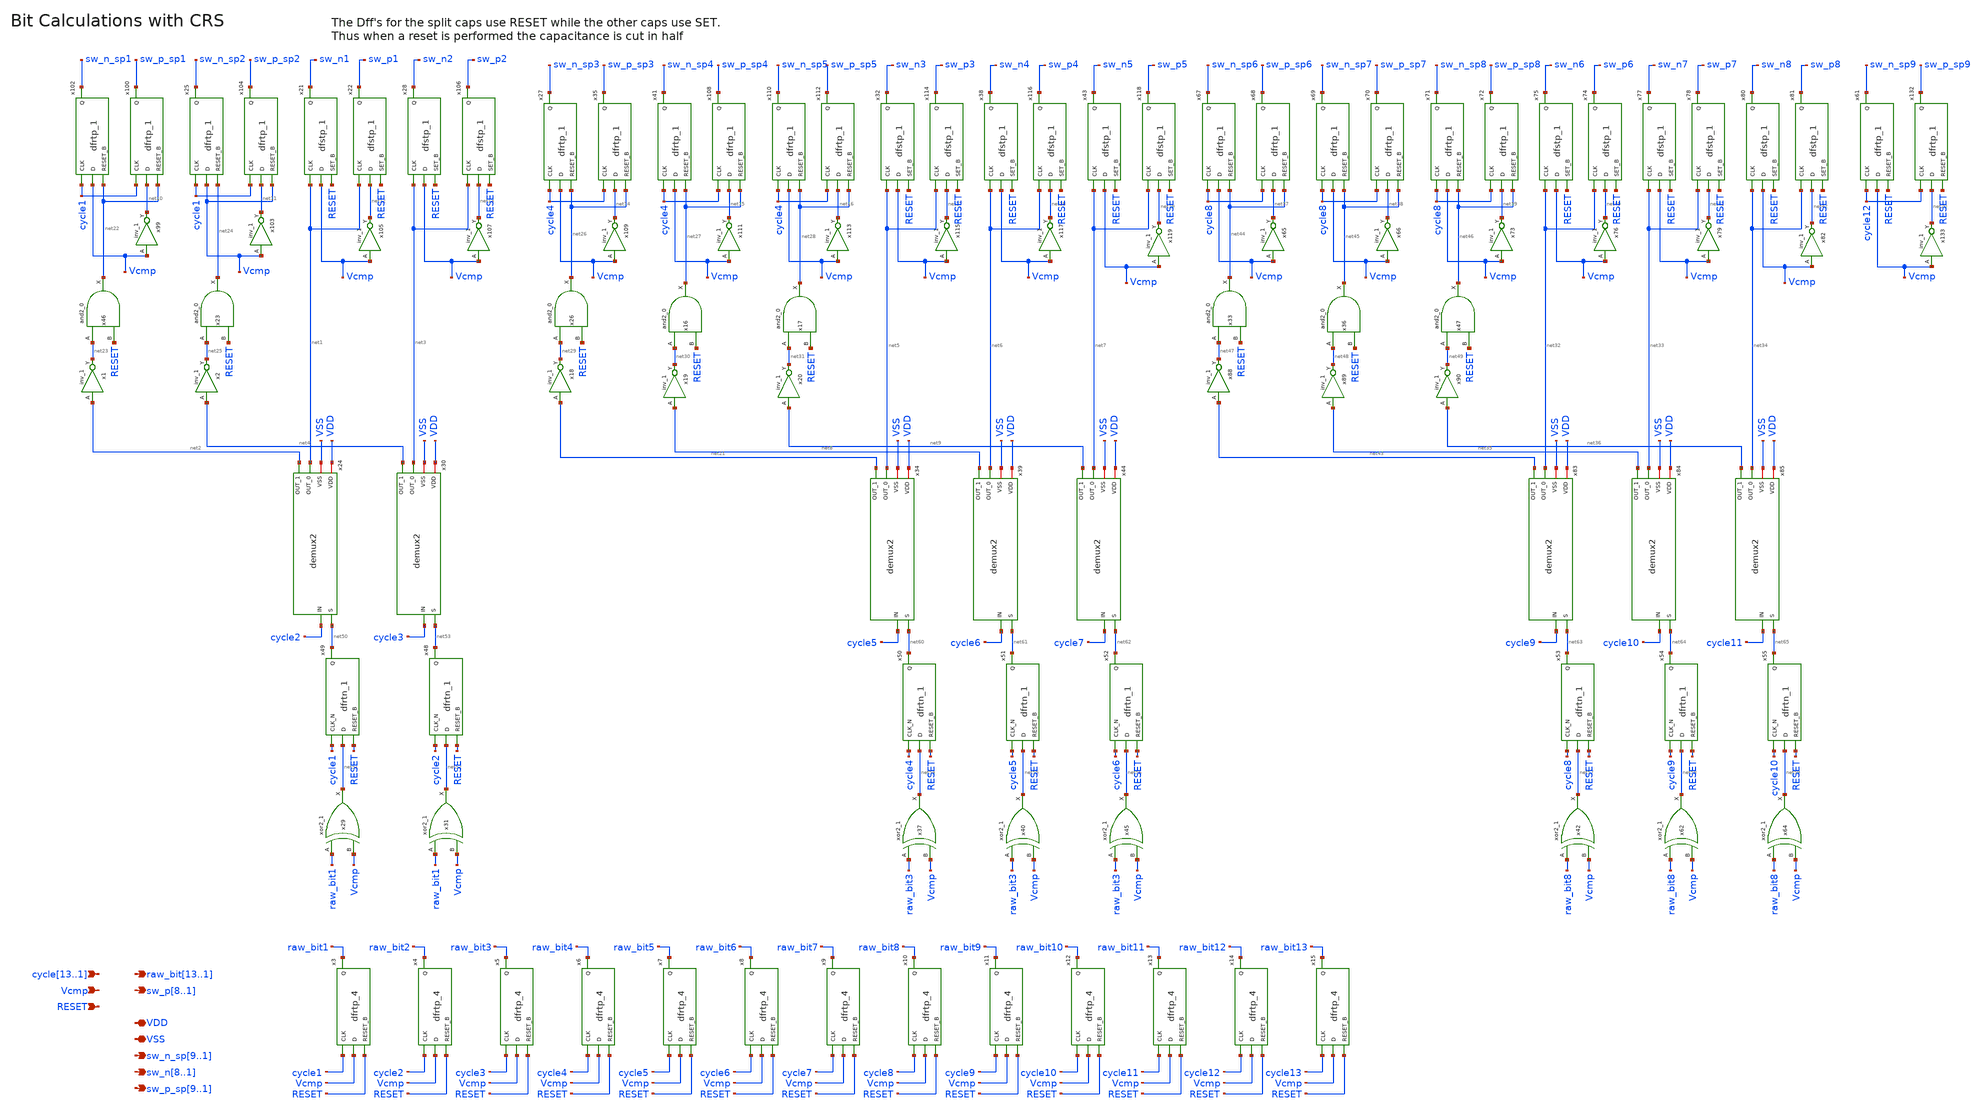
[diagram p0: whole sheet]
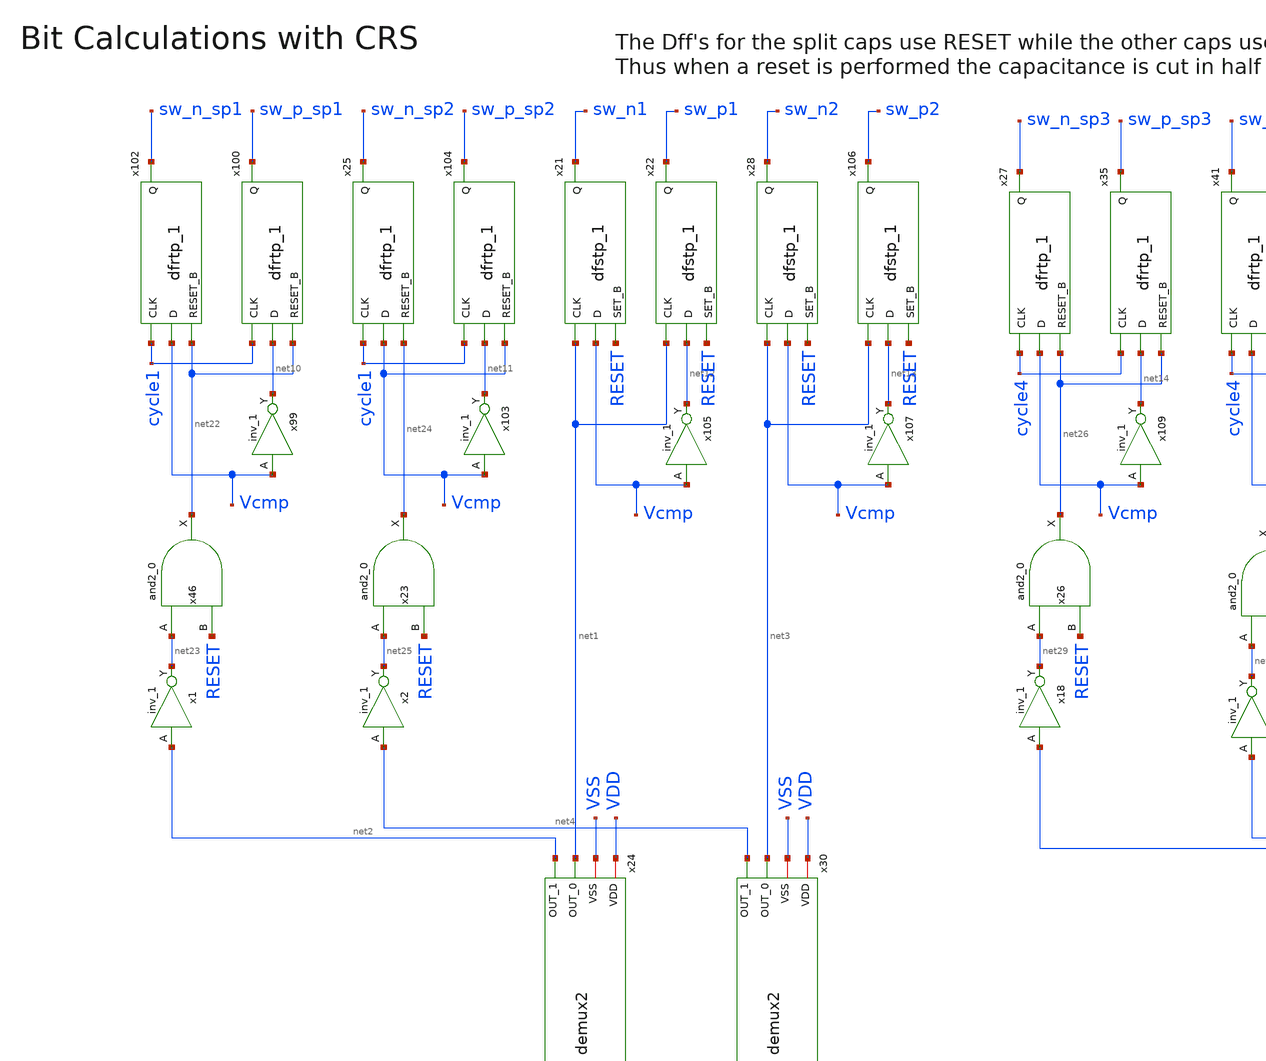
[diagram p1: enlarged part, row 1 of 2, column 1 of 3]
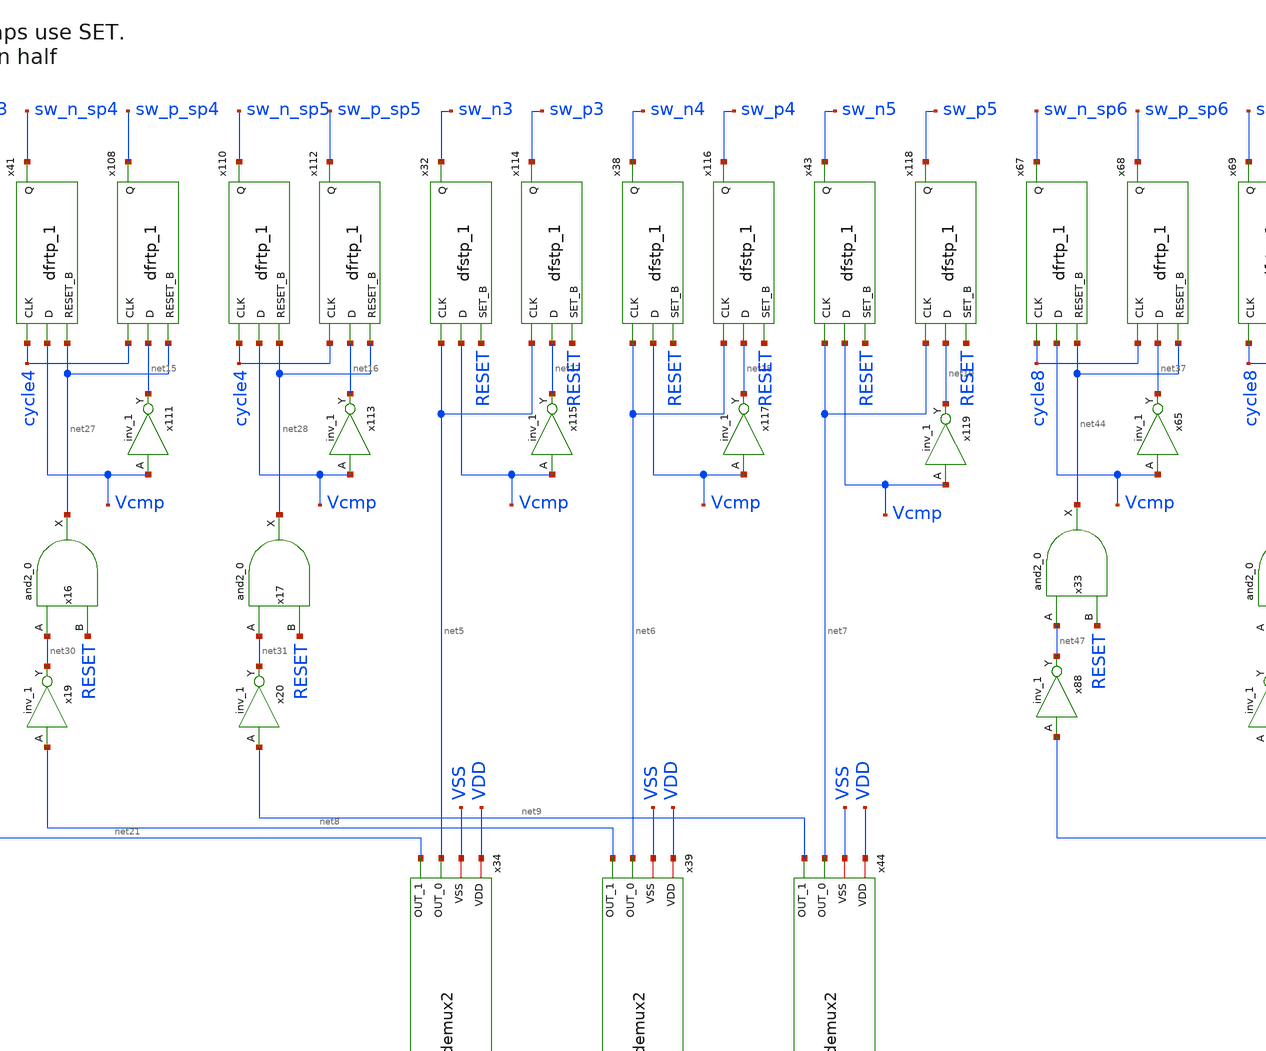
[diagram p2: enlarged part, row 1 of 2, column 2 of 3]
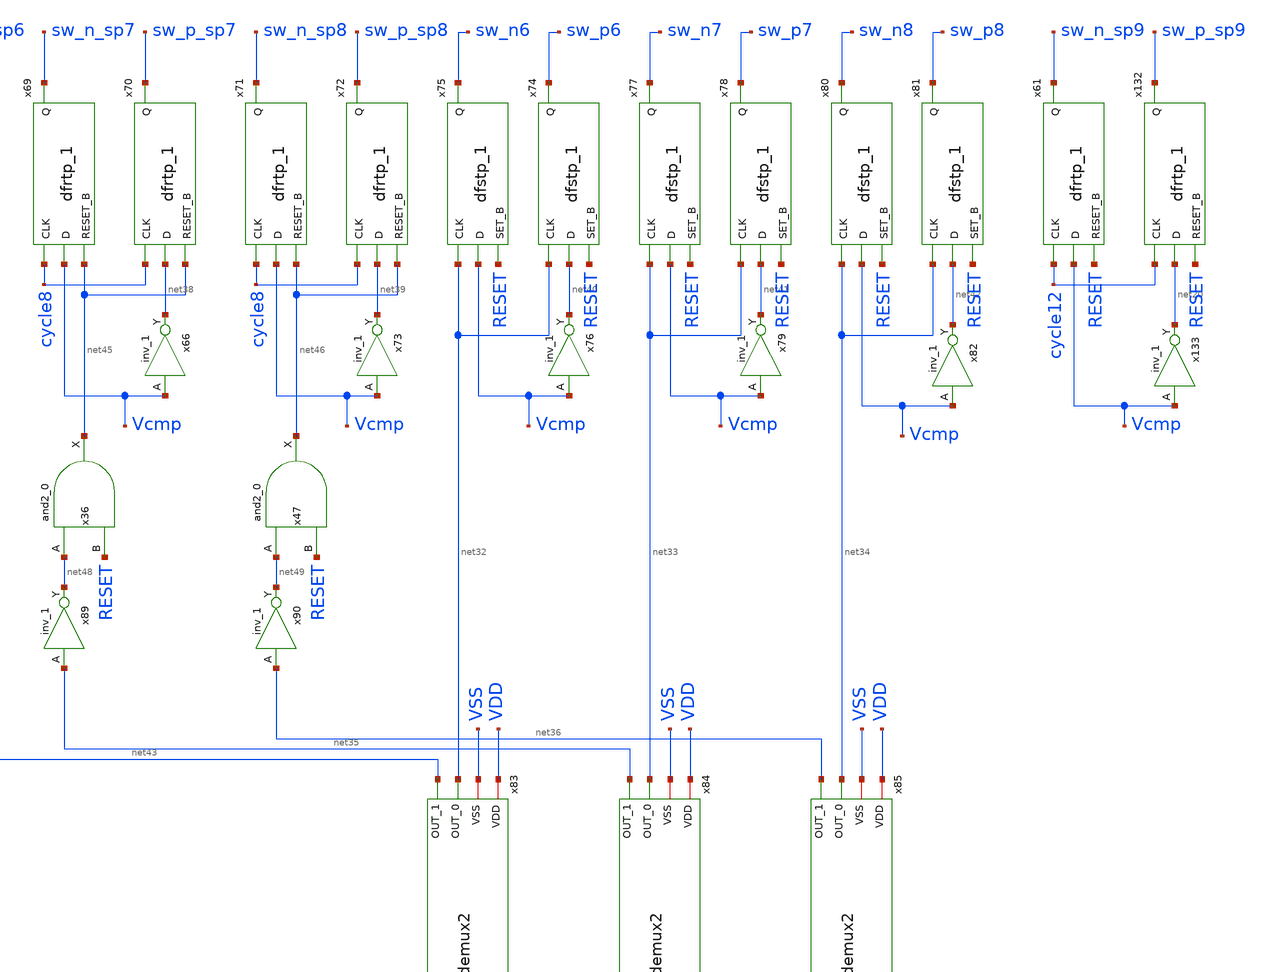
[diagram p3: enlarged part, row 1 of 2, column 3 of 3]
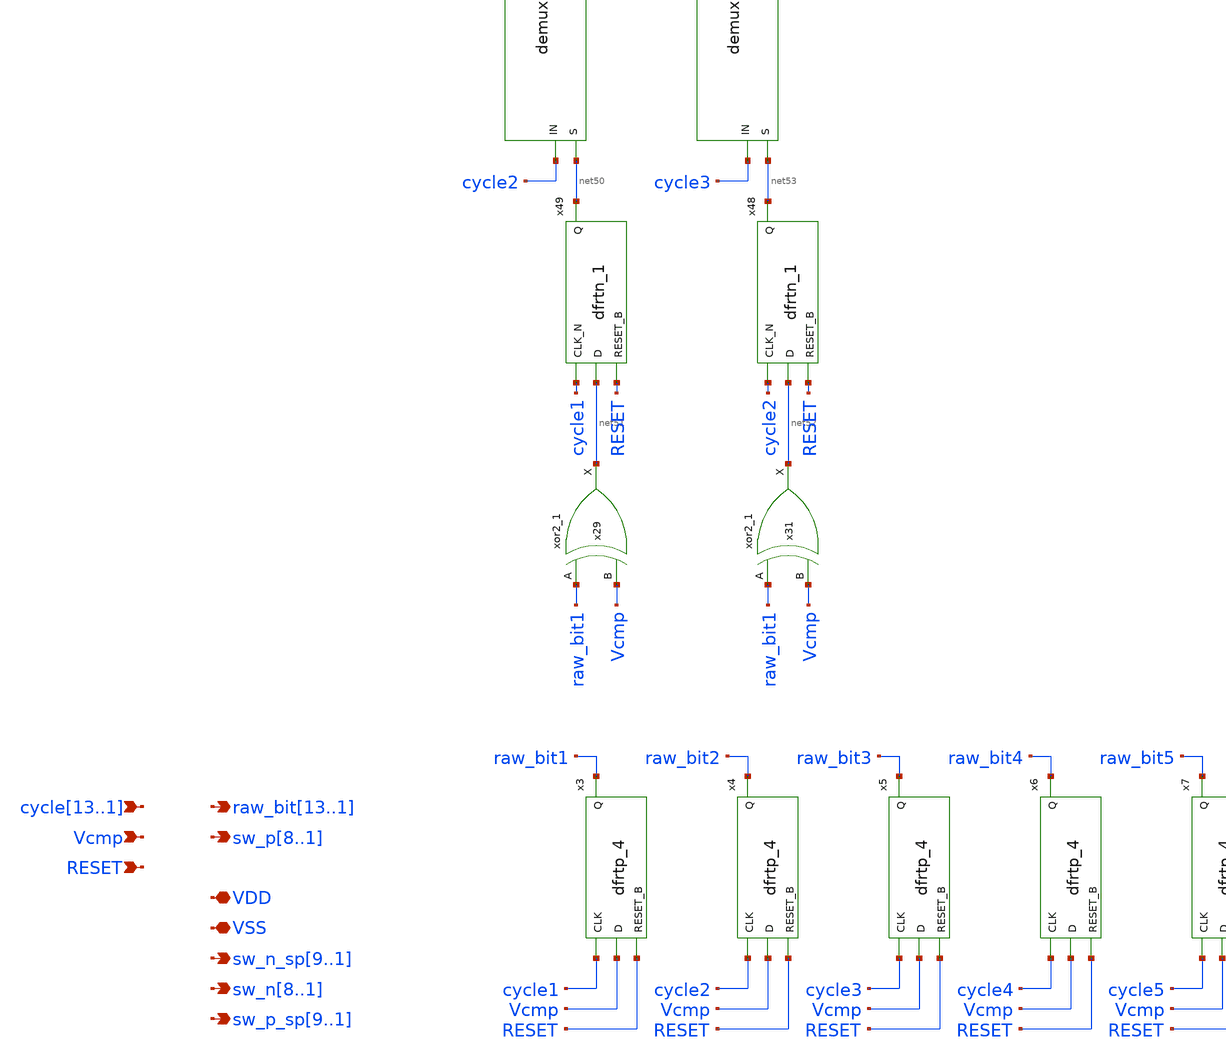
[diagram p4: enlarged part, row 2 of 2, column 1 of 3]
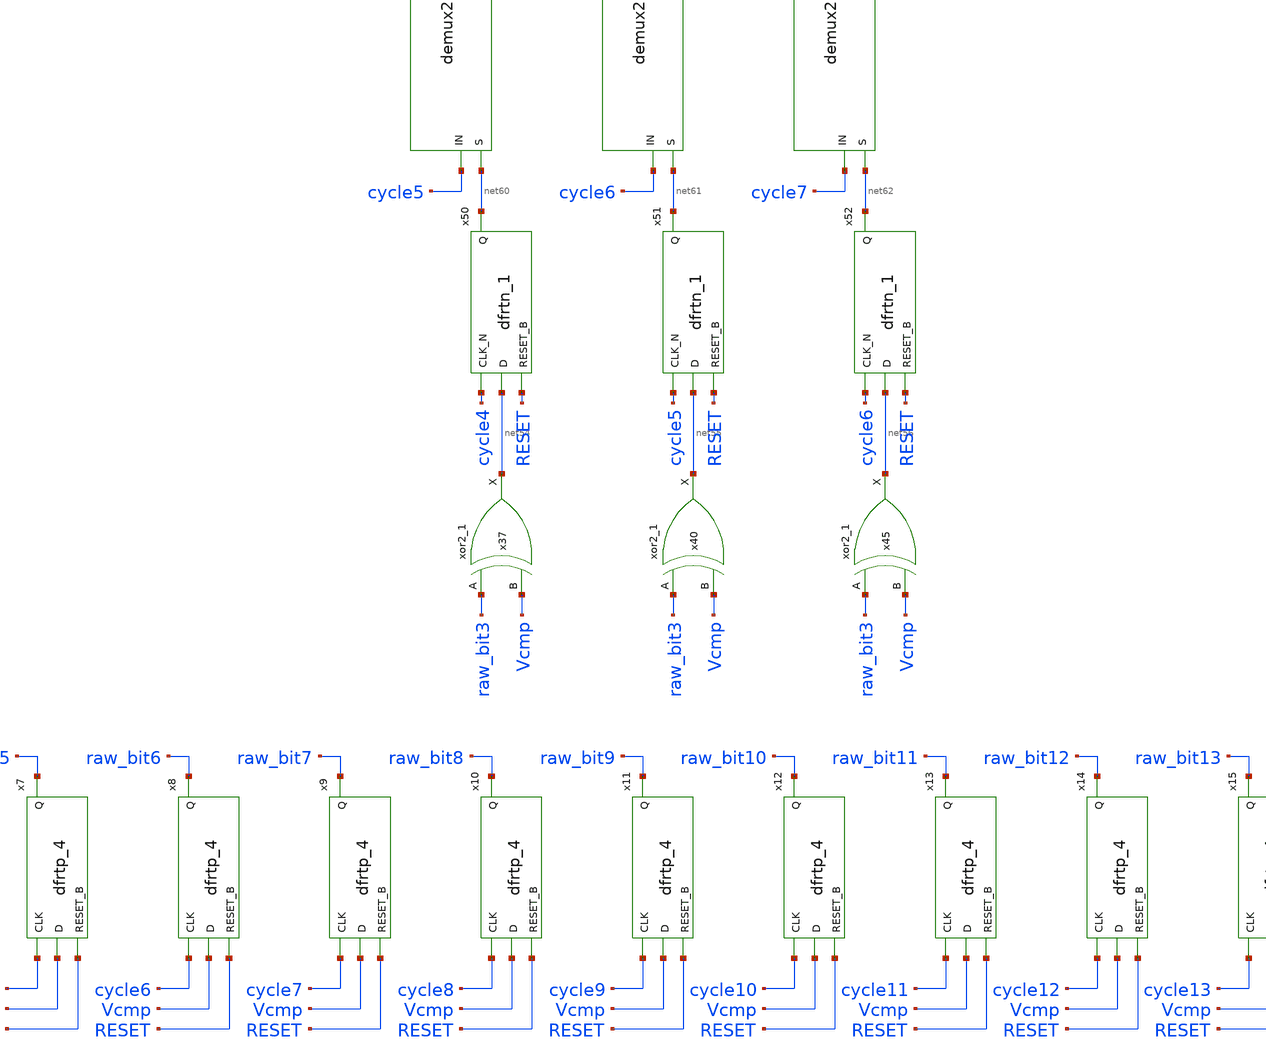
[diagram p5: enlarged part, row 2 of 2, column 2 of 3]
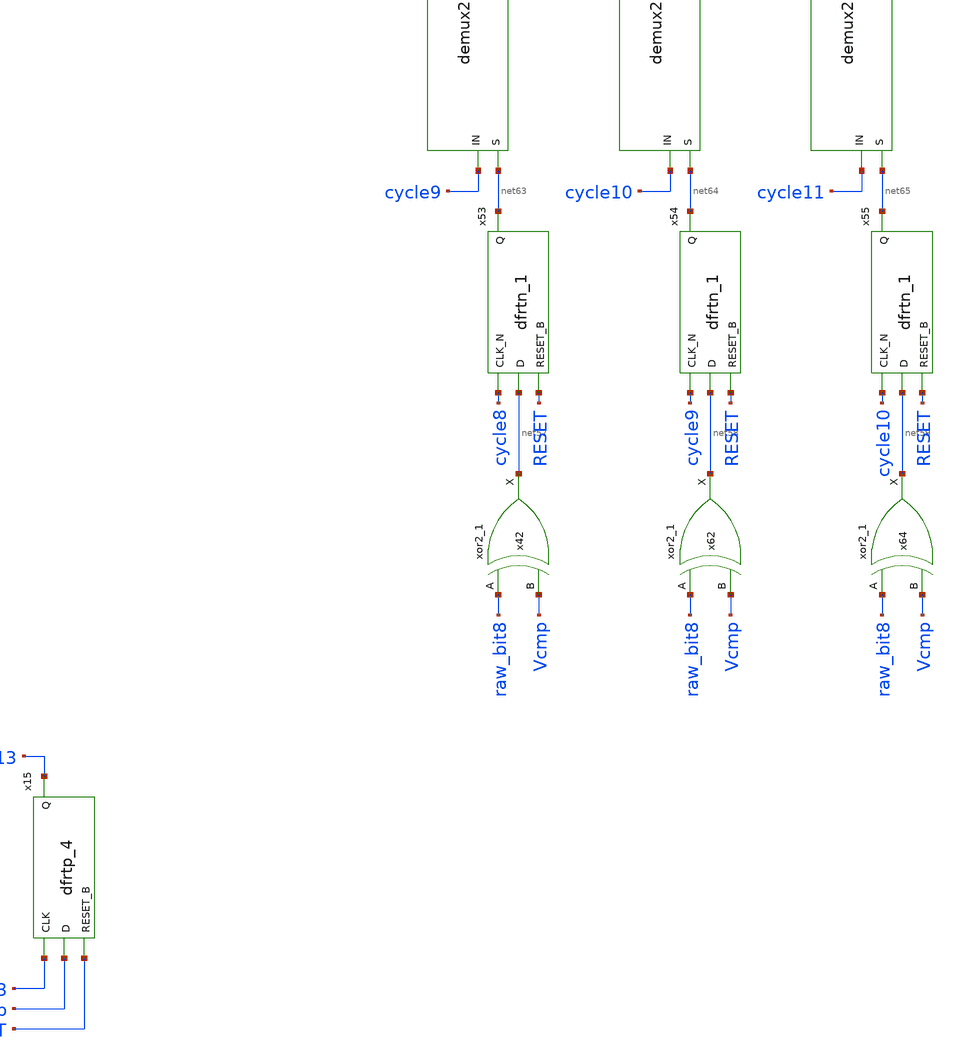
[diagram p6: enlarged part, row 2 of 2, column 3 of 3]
** sch_path: xschem/src/raw_bit_calculator/raw_bit_calculator.sch
**.subckt raw_bit_calculator
*+ cycle13,cycle12,cycle11,cycle10,cycle9,cycle8,cycle7,cycle6,cycle5,cycle4,cycle3,cycle2,cycle1 sw_n_sp9,sw_n_sp8,sw_n_sp7,sw_n_sp6,sw_n_sp5,sw_n_sp4,sw_n_sp3,sw_n_sp2,sw_n_sp1 VSS VDD
*+ sw_n8,sw_n7,sw_n6,sw_n5,sw_n4,sw_n3,sw_n2,sw_n1 sw_p_sp9,sw_p_sp8,sw_p_sp7,sw_p_sp6,sw_p_sp5,sw_p_sp4,sw_p_sp3,sw_p_sp2,sw_p_sp1
*+ sw_p8,sw_p7,sw_p6,sw_p5,sw_p4,sw_p3,sw_p2,sw_p1 Vcmp RESET
*+ raw_bit13,raw_bit12,raw_bit11,raw_bit10,raw_bit9,raw_bit8,raw_bit7,raw_bit6,raw_bit5,raw_bit4,raw_bit3,raw_bit2,raw_bit1
*.ipin
*+ cycle13,cycle12,cycle11,cycle10,cycle9,cycle8,cycle7,cycle6,cycle5,cycle4,cycle3,cycle2,cycle1
*.opin sw_n_sp9,sw_n_sp8,sw_n_sp7,sw_n_sp6,sw_n_sp5,sw_n_sp4,sw_n_sp3,sw_n_sp2,sw_n_sp1
*.iopin VSS
*.iopin VDD
*.opin sw_n8,sw_n7,sw_n6,sw_n5,sw_n4,sw_n3,sw_n2,sw_n1
*.opin sw_p_sp9,sw_p_sp8,sw_p_sp7,sw_p_sp6,sw_p_sp5,sw_p_sp4,sw_p_sp3,sw_p_sp2,sw_p_sp1
*.opin sw_p8,sw_p7,sw_p6,sw_p5,sw_p4,sw_p3,sw_p2,sw_p1
*.ipin Vcmp
*.ipin RESET
*.opin
*+ raw_bit13,raw_bit12,raw_bit11,raw_bit10,raw_bit9,raw_bit8,raw_bit7,raw_bit6,raw_bit5,raw_bit4,raw_bit3,raw_bit2,raw_bit1
x29 raw_bit1 Vcmp VSS VSS VDD VDD net51 sky130_fd_sc_hd__xor2_1
x31 raw_bit1 Vcmp VSS VSS VDD VDD net52 sky130_fd_sc_hd__xor2_1
x37 raw_bit3 Vcmp VSS VSS VDD VDD net54 sky130_fd_sc_hd__xor2_1
x40 raw_bit3 Vcmp VSS VSS VDD VDD net55 sky130_fd_sc_hd__xor2_1
x45 raw_bit3 Vcmp VSS VSS VDD VDD net56 sky130_fd_sc_hd__xor2_1
x100 cycle1 net10 net22 VSS VSS VDD VDD sw_p_sp1 sky130_fd_sc_hd__dfrtp_1
x99 Vcmp VSS VSS VDD VDD net10 sky130_fd_sc_hd__inv_1
x102 cycle1 Vcmp net22 VSS VSS VDD VDD sw_n_sp1 sky130_fd_sc_hd__dfrtp_1
x25 cycle1 Vcmp net24 VSS VSS VDD VDD sw_n_sp2 sky130_fd_sc_hd__dfrtp_1
x103 Vcmp VSS VSS VDD VDD net11 sky130_fd_sc_hd__inv_1
x104 cycle1 net11 Vcmp VSS VSS VDD VDD sw_p_sp2 sky130_fd_sc_hd__dfrtp_1
x21 net1 Vcmp RESET VSS VSS VDD VDD sw_n1 sky130_fd_sc_hd__dfstp_1
x22 net1 net12 RESET VSS VSS VDD VDD sw_p1 sky130_fd_sc_hd__dfstp_1
x105 Vcmp VSS VSS VDD VDD net12 sky130_fd_sc_hd__inv_1
x28 net3 Vcmp RESET VSS VSS VDD VDD sw_n2 sky130_fd_sc_hd__dfstp_1
x106 net3 net13 RESET VSS VSS VDD VDD sw_p2 sky130_fd_sc_hd__dfstp_1
x107 Vcmp VSS VSS VDD VDD net13 sky130_fd_sc_hd__inv_1
x109 Vcmp VSS VSS VDD VDD net14 sky130_fd_sc_hd__inv_1
x111 Vcmp VSS VSS VDD VDD net15 sky130_fd_sc_hd__inv_1
x27 cycle4 Vcmp net26 VSS VSS VDD VDD sw_n_sp3 sky130_fd_sc_hd__dfrtp_1
x35 cycle4 net14 net26 VSS VSS VDD VDD sw_p_sp3 sky130_fd_sc_hd__dfrtp_1
x41 cycle4 Vcmp net27 VSS VSS VDD VDD sw_n_sp4 sky130_fd_sc_hd__dfrtp_1
x108 cycle4 net15 net27 VSS VSS VDD VDD sw_p_sp4 sky130_fd_sc_hd__dfrtp_1
x110 cycle4 Vcmp net28 VSS VSS VDD VDD sw_n_sp5 sky130_fd_sc_hd__dfrtp_1
x112 cycle4 net16 net28 VSS VSS VDD VDD sw_p_sp5 sky130_fd_sc_hd__dfrtp_1
x113 Vcmp VSS VSS VDD VDD net16 sky130_fd_sc_hd__inv_1
x114 net5 net17 RESET VSS VSS VDD VDD sw_p3 sky130_fd_sc_hd__dfstp_1
x32 net5 Vcmp RESET VSS VSS VDD VDD sw_n3 sky130_fd_sc_hd__dfstp_1
x115 Vcmp VSS VSS VDD VDD net17 sky130_fd_sc_hd__inv_1
x38 net6 Vcmp RESET VSS VSS VDD VDD sw_n4 sky130_fd_sc_hd__dfstp_1
x116 net6 net18 RESET VSS VSS VDD VDD sw_p4 sky130_fd_sc_hd__dfstp_1
x117 Vcmp VSS VSS VDD VDD net18 sky130_fd_sc_hd__inv_1
x43 net7 Vcmp RESET VSS VSS VDD VDD sw_n5 sky130_fd_sc_hd__dfstp_1
x118 net7 net19 RESET VSS VSS VDD VDD sw_p5 sky130_fd_sc_hd__dfstp_1
x119 Vcmp VSS VSS VDD VDD net19 sky130_fd_sc_hd__inv_1
x132 cycle12 net20 RESET VSS VSS VDD VDD sw_p_sp9 sky130_fd_sc_hd__dfrtp_1
x133 Vcmp VSS VSS VDD VDD net20 sky130_fd_sc_hd__inv_1
x61 cycle12 Vcmp RESET VSS VSS VDD VDD sw_n_sp9 sky130_fd_sc_hd__dfrtp_1
x24 net50 VDD VSS net1 cycle2 net2 demux2
x30 net53 VDD VSS net3 cycle3 net4 demux2
x34 net60 VDD VSS net5 cycle5 net21 demux2
x39 net61 VDD VSS net6 cycle6 net8 demux2
x44 net62 VDD VSS net7 cycle7 net9 demux2
x1 net2 VSS VSS VDD VDD net23 sky130_fd_sc_hd__inv_1
x2 net4 VSS VSS VDD VDD net25 sky130_fd_sc_hd__inv_1
x3 cycle1 Vcmp RESET VSS VSS VDD VDD raw_bit1 sky130_fd_sc_hd__dfrtp_4
x4 cycle2 Vcmp RESET VSS VSS VDD VDD raw_bit2 sky130_fd_sc_hd__dfrtp_4
x5 cycle3 Vcmp RESET VSS VSS VDD VDD raw_bit3 sky130_fd_sc_hd__dfrtp_4
x6 cycle4 Vcmp RESET VSS VSS VDD VDD raw_bit4 sky130_fd_sc_hd__dfrtp_4
x7 cycle5 Vcmp RESET VSS VSS VDD VDD raw_bit5 sky130_fd_sc_hd__dfrtp_4
x8 cycle6 Vcmp RESET VSS VSS VDD VDD raw_bit6 sky130_fd_sc_hd__dfrtp_4
x9 cycle7 Vcmp RESET VSS VSS VDD VDD raw_bit7 sky130_fd_sc_hd__dfrtp_4
x10 cycle8 Vcmp RESET VSS VSS VDD VDD raw_bit8 sky130_fd_sc_hd__dfrtp_4
x11 cycle9 Vcmp RESET VSS VSS VDD VDD raw_bit9 sky130_fd_sc_hd__dfrtp_4
x12 cycle10 Vcmp RESET VSS VSS VDD VDD raw_bit10 sky130_fd_sc_hd__dfrtp_4
x13 cycle11 Vcmp RESET VSS VSS VDD VDD raw_bit11 sky130_fd_sc_hd__dfrtp_4
x14 cycle12 Vcmp RESET VSS VSS VDD VDD raw_bit12 sky130_fd_sc_hd__dfrtp_4
x15 cycle13 Vcmp RESET VSS VSS VDD VDD raw_bit13 sky130_fd_sc_hd__dfrtp_4
x18 net21 VSS VSS VDD VDD net29 sky130_fd_sc_hd__inv_1
x19 net8 VSS VSS VDD VDD net30 sky130_fd_sc_hd__inv_1
x20 net9 VSS VSS VDD VDD net31 sky130_fd_sc_hd__inv_1
x42 raw_bit8 Vcmp VSS VSS VDD VDD net57 sky130_fd_sc_hd__xor2_1
x62 raw_bit8 Vcmp VSS VSS VDD VDD net58 sky130_fd_sc_hd__xor2_1
x64 raw_bit8 Vcmp VSS VSS VDD VDD net59 sky130_fd_sc_hd__xor2_1
x65 Vcmp VSS VSS VDD VDD net37 sky130_fd_sc_hd__inv_1
x66 Vcmp VSS VSS VDD VDD net38 sky130_fd_sc_hd__inv_1
x67 cycle8 Vcmp net44 VSS VSS VDD VDD sw_n_sp6 sky130_fd_sc_hd__dfrtp_1
x68 cycle8 net37 net44 VSS VSS VDD VDD sw_p_sp6 sky130_fd_sc_hd__dfrtp_1
x69 cycle8 Vcmp net45 VSS VSS VDD VDD sw_n_sp7 sky130_fd_sc_hd__dfrtp_1
x70 cycle8 net38 net45 VSS VSS VDD VDD sw_p_sp7 sky130_fd_sc_hd__dfrtp_1
x71 cycle8 Vcmp net46 VSS VSS VDD VDD sw_n_sp8 sky130_fd_sc_hd__dfrtp_1
x72 cycle8 net39 net46 VSS VSS VDD VDD sw_p_sp8 sky130_fd_sc_hd__dfrtp_1
x73 Vcmp VSS VSS VDD VDD net39 sky130_fd_sc_hd__inv_1
x74 net32 net40 RESET VSS VSS VDD VDD sw_p6 sky130_fd_sc_hd__dfstp_1
x75 net32 Vcmp RESET VSS VSS VDD VDD sw_n6 sky130_fd_sc_hd__dfstp_1
x76 Vcmp VSS VSS VDD VDD net40 sky130_fd_sc_hd__inv_1
x77 net33 Vcmp RESET VSS VSS VDD VDD sw_n7 sky130_fd_sc_hd__dfstp_1
x78 net33 net41 RESET VSS VSS VDD VDD sw_p7 sky130_fd_sc_hd__dfstp_1
x79 Vcmp VSS VSS VDD VDD net41 sky130_fd_sc_hd__inv_1
x80 net34 Vcmp RESET VSS VSS VDD VDD sw_n8 sky130_fd_sc_hd__dfstp_1
x81 net34 net42 RESET VSS VSS VDD VDD sw_p8 sky130_fd_sc_hd__dfstp_1
x82 Vcmp VSS VSS VDD VDD net42 sky130_fd_sc_hd__inv_1
x83 net63 VDD VSS net32 cycle9 net43 demux2
x84 net64 VDD VSS net33 cycle10 net35 demux2
x85 net65 VDD VSS net34 cycle11 net36 demux2
x88 net43 VSS VSS VDD VDD net47 sky130_fd_sc_hd__inv_1
x89 net35 VSS VSS VDD VDD net48 sky130_fd_sc_hd__inv_1
x90 net36 VSS VSS VDD VDD net49 sky130_fd_sc_hd__inv_1
x46 net23 RESET VSS VSS VDD VDD net22 sky130_fd_sc_hd__and2_0
x23 net25 RESET VSS VSS VDD VDD net24 sky130_fd_sc_hd__and2_0
x26 net29 RESET VSS VSS VDD VDD net26 sky130_fd_sc_hd__and2_0
x16 net30 RESET VSS VSS VDD VDD net27 sky130_fd_sc_hd__and2_0
x17 net31 RESET VSS VSS VDD VDD net28 sky130_fd_sc_hd__and2_0
x33 net47 RESET VSS VSS VDD VDD net44 sky130_fd_sc_hd__and2_0
x36 net48 RESET VSS VSS VDD VDD net45 sky130_fd_sc_hd__and2_0
x47 net49 RESET VSS VSS VDD VDD net46 sky130_fd_sc_hd__and2_0
x49 cycle1 net51 RESET VSS VSS VDD VDD net50 sky130_fd_sc_hd__dfrtn_1
x48 cycle2 net52 RESET VSS VSS VDD VDD net53 sky130_fd_sc_hd__dfrtn_1
x50 cycle4 net54 RESET VSS VSS VDD VDD net60 sky130_fd_sc_hd__dfrtn_1
x51 cycle5 net55 RESET VSS VSS VDD VDD net61 sky130_fd_sc_hd__dfrtn_1
x52 cycle6 net56 RESET VSS VSS VDD VDD net62 sky130_fd_sc_hd__dfrtn_1
x53 cycle8 net57 RESET VSS VSS VDD VDD net63 sky130_fd_sc_hd__dfrtn_1
x54 cycle9 net58 RESET VSS VSS VDD VDD net64 sky130_fd_sc_hd__dfrtn_1
x55 cycle10 net59 RESET VSS VSS VDD VDD net65 sky130_fd_sc_hd__dfrtn_1
**.ends

* expanding   symbol:  src/demux2/demux2.sym # of pins=6
** sym_path: xschem/src/demux2/demux2.sym
** sch_path: xschem/src/demux2/demux2.sch
.subckt demux2 S VDD VSS OUT_0 IN OUT_1
*.ipin S
*.opin OUT_0
*.ipin IN
*.opin OUT_1
*.iopin VDD
*.iopin VSS
x1 net1 IN VSS VSS VDD VDD OUT_0 sky130_fd_sc_hd__and2_0
x2 S IN VSS VSS VDD VDD OUT_1 sky130_fd_sc_hd__and2_0
x3 S VSS VSS VDD VDD net1 sky130_fd_sc_hd__inv_1
.ends

.end
